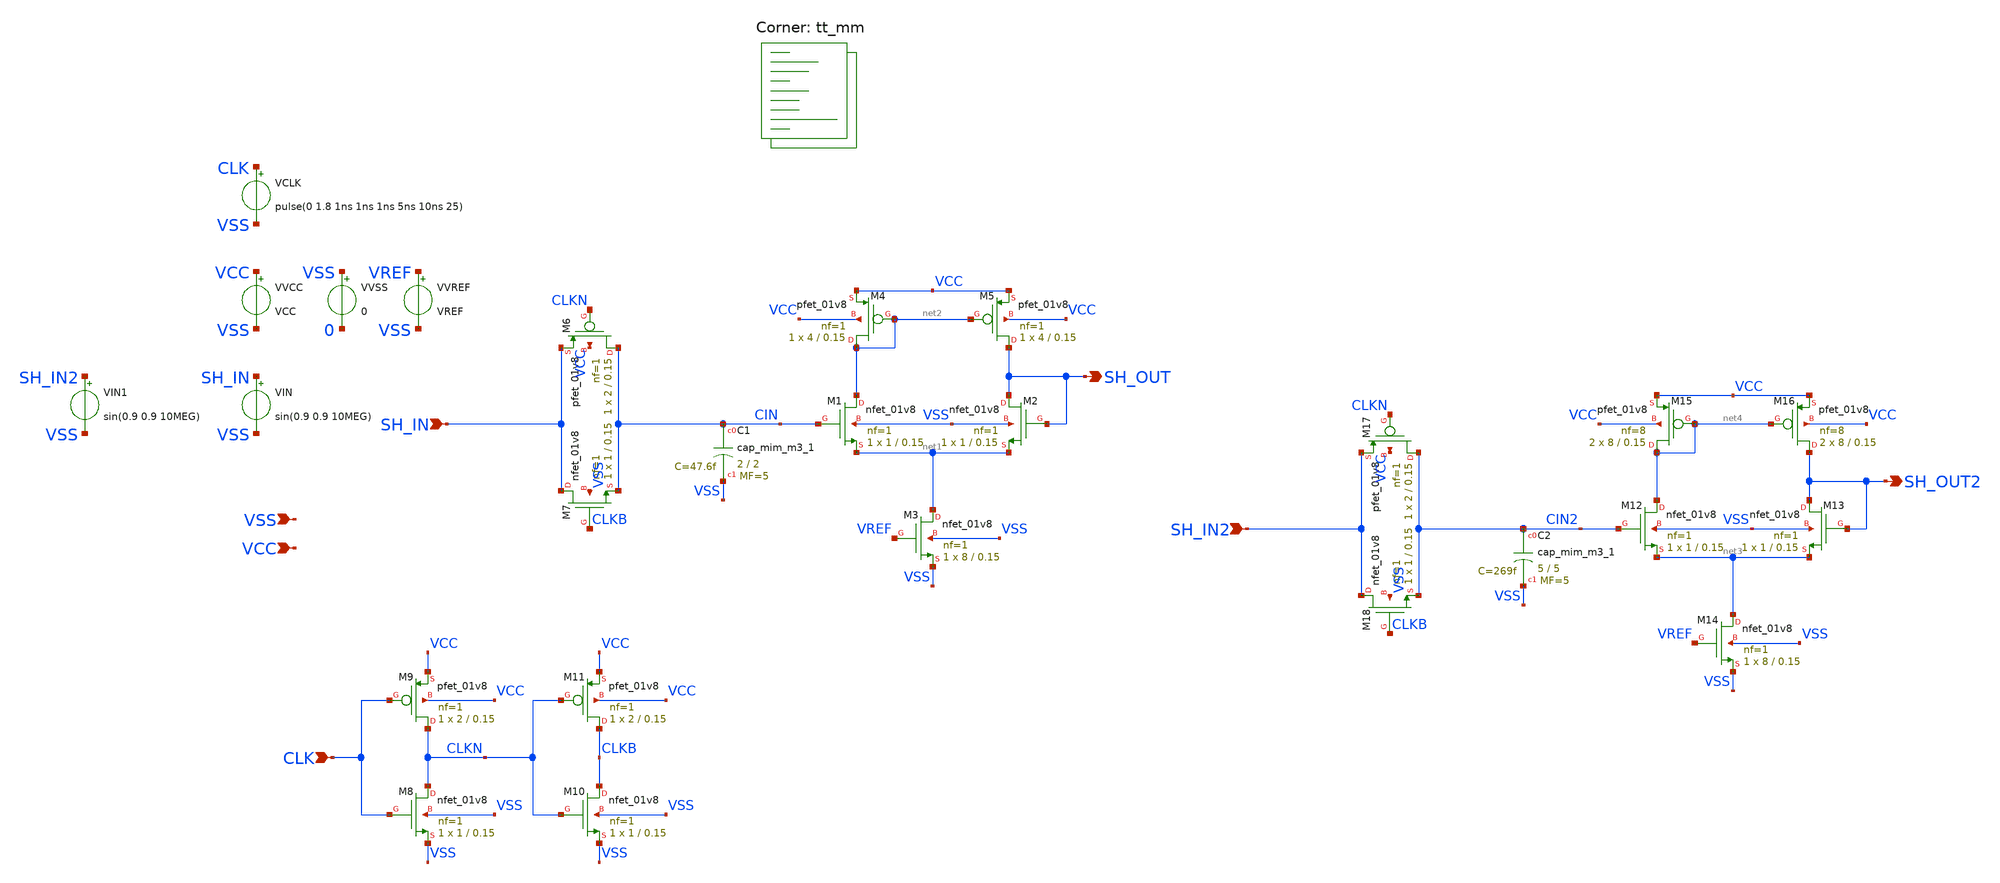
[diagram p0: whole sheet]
** sch_path: xschem/Sample_and_Hold.sch
**.subckt Sample_and_Hold SH_IN CLK SH_OUT VSS VCC SH_IN2 SH_OUT2
*.ipin SH_IN
*.ipin CLK
*.opin SH_OUT
*.ipin VSS
*.ipin VCC
*.ipin SH_IN2
*.opin SH_OUT2
XM1 net2 CIN net1 VSS sky130_fd_pr__nfet_01v8 L=0.15 W=1 nf=1 ad='int((nf+1)/2) * W/nf * 0.29' as='int((nf+2)/2) * W/nf * 0.29'
+ pd='2*int((nf+1)/2) * (W/nf + 0.29)' ps='2*int((nf+2)/2) * (W/nf + 0.29)' nrd='0.29 / W' nrs='0.29 / W'
+ sa=0 sb=0 sd=0 mult=1 m=1
XM2 SH_OUT SH_OUT net1 VSS sky130_fd_pr__nfet_01v8 L=0.15 W=1 nf=1 ad='int((nf+1)/2) * W/nf * 0.29' as='int((nf+2)/2) * W/nf * 0.29'
+ pd='2*int((nf+1)/2) * (W/nf + 0.29)' ps='2*int((nf+2)/2) * (W/nf + 0.29)' nrd='0.29 / W' nrs='0.29 / W'
+ sa=0 sb=0 sd=0 mult=1 m=1
XM3 net1 VREF VSS VSS sky130_fd_pr__nfet_01v8 L=0.15 W=8 nf=1 ad='int((nf+1)/2) * W/nf * 0.29' as='int((nf+2)/2) * W/nf * 0.29'
+ pd='2*int((nf+1)/2) * (W/nf + 0.29)' ps='2*int((nf+2)/2) * (W/nf + 0.29)' nrd='0.29 / W' nrs='0.29 / W'
+ sa=0 sb=0 sd=0 mult=1 m=1
XM4 net2 net2 VCC VCC sky130_fd_pr__pfet_01v8 L=0.15 W=4 nf=1 ad='int((nf+1)/2) * W/nf * 0.29' as='int((nf+2)/2) * W/nf * 0.29'
+ pd='2*int((nf+1)/2) * (W/nf + 0.29)' ps='2*int((nf+2)/2) * (W/nf + 0.29)' nrd='0.29 / W' nrs='0.29 / W'
+ sa=0 sb=0 sd=0 mult=1 m=1
XM5 SH_OUT net2 VCC VCC sky130_fd_pr__pfet_01v8 L=0.15 W=4 nf=1 ad='int((nf+1)/2) * W/nf * 0.29' as='int((nf+2)/2) * W/nf * 0.29'
+ pd='2*int((nf+1)/2) * (W/nf + 0.29)' ps='2*int((nf+2)/2) * (W/nf + 0.29)' nrd='0.29 / W' nrs='0.29 / W'
+ sa=0 sb=0 sd=0 mult=1 m=1
XC1 CIN VSS sky130_fd_pr__cap_mim_m3_1 W=2 L=2 MF=5 m=5
XM6 CIN CLKN SH_IN VCC sky130_fd_pr__pfet_01v8 L=0.15 W=2 nf=1 ad='int((nf+1)/2) * W/nf * 0.29' as='int((nf+2)/2) * W/nf * 0.29'
+ pd='2*int((nf+1)/2) * (W/nf + 0.29)' ps='2*int((nf+2)/2) * (W/nf + 0.29)' nrd='0.29 / W' nrs='0.29 / W'
+ sa=0 sb=0 sd=0 mult=1 m=1
XM7 SH_IN CLKB CIN VSS sky130_fd_pr__nfet_01v8 L=0.15 W=1 nf=1 ad='int((nf+1)/2) * W/nf * 0.29' as='int((nf+2)/2) * W/nf * 0.29'
+ pd='2*int((nf+1)/2) * (W/nf + 0.29)' ps='2*int((nf+2)/2) * (W/nf + 0.29)' nrd='0.29 / W' nrs='0.29 / W'
+ sa=0 sb=0 sd=0 mult=1 m=1
VCLK CLK VSS pulse(0 1.8 1ns 1ns 1ns 5ns 10ns 25)
VVCC VCC VSS VCC
VVSS VSS 0 0
VIN SH_IN VSS sin(0.9 0.9 10MEG)
VVREF VREF VSS VREF
XM8 CLKN CLK VSS VSS sky130_fd_pr__nfet_01v8 L=0.15 W=1 nf=1 ad='int((nf+1)/2) * W/nf * 0.29' as='int((nf+2)/2) * W/nf * 0.29'
+ pd='2*int((nf+1)/2) * (W/nf + 0.29)' ps='2*int((nf+2)/2) * (W/nf + 0.29)' nrd='0.29 / W' nrs='0.29 / W'
+ sa=0 sb=0 sd=0 mult=1 m=1
XM9 CLKN CLK VCC VCC sky130_fd_pr__pfet_01v8 L=0.15 W=2 nf=1 ad='int((nf+1)/2) * W/nf * 0.29' as='int((nf+2)/2) * W/nf * 0.29'
+ pd='2*int((nf+1)/2) * (W/nf + 0.29)' ps='2*int((nf+2)/2) * (W/nf + 0.29)' nrd='0.29 / W' nrs='0.29 / W'
+ sa=0 sb=0 sd=0 mult=1 m=1
XM10 CLKB CLKN VSS VSS sky130_fd_pr__nfet_01v8 L=0.15 W=1 nf=1 ad='int((nf+1)/2) * W/nf * 0.29' as='int((nf+2)/2) * W/nf * 0.29'
+ pd='2*int((nf+1)/2) * (W/nf + 0.29)' ps='2*int((nf+2)/2) * (W/nf + 0.29)' nrd='0.29 / W' nrs='0.29 / W'
+ sa=0 sb=0 sd=0 mult=1 m=1
XM11 CLKB CLKN VCC VCC sky130_fd_pr__pfet_01v8 L=0.15 W=2 nf=1 ad='int((nf+1)/2) * W/nf * 0.29' as='int((nf+2)/2) * W/nf * 0.29'
+ pd='2*int((nf+1)/2) * (W/nf + 0.29)' ps='2*int((nf+2)/2) * (W/nf + 0.29)' nrd='0.29 / W' nrs='0.29 / W'
+ sa=0 sb=0 sd=0 mult=1 m=1
XM12 net4 CIN2 net3 VSS sky130_fd_pr__nfet_01v8 L=0.15 W=1 nf=1 ad='int((nf+1)/2) * W/nf * 0.29' as='int((nf+2)/2) * W/nf * 0.29'
+ pd='2*int((nf+1)/2) * (W/nf + 0.29)' ps='2*int((nf+2)/2) * (W/nf + 0.29)' nrd='0.29 / W' nrs='0.29 / W'
+ sa=0 sb=0 sd=0 mult=1 m=1
XM13 SH_OUT2 SH_OUT2 net3 VSS sky130_fd_pr__nfet_01v8 L=0.15 W=1 nf=1 ad='int((nf+1)/2) * W/nf * 0.29'
+ as='int((nf+2)/2) * W/nf * 0.29' pd='2*int((nf+1)/2) * (W/nf + 0.29)' ps='2*int((nf+2)/2) * (W/nf + 0.29)'
+ nrd='0.29 / W' nrs='0.29 / W' sa=0 sb=0 sd=0 mult=1 m=1
XM14 net3 VREF VSS VSS sky130_fd_pr__nfet_01v8 L=0.15 W=8 nf=1 ad='int((nf+1)/2) * W/nf * 0.29' as='int((nf+2)/2) * W/nf * 0.29'
+ pd='2*int((nf+1)/2) * (W/nf + 0.29)' ps='2*int((nf+2)/2) * (W/nf + 0.29)' nrd='0.29 / W' nrs='0.29 / W'
+ sa=0 sb=0 sd=0 mult=1 m=1
XM15 net4 net4 VCC VCC sky130_fd_pr__pfet_01v8 L=0.15 W=8 nf=8 ad='int((nf+1)/2) * W/nf * 0.29' as='int((nf+2)/2) * W/nf * 0.29'
+ pd='2*int((nf+1)/2) * (W/nf + 0.29)' ps='2*int((nf+2)/2) * (W/nf + 0.29)' nrd='0.29 / W' nrs='0.29 / W'
+ sa=0 sb=0 sd=0 mult=2 m=2
XM16 SH_OUT2 net4 VCC VCC sky130_fd_pr__pfet_01v8 L=0.15 W=8 nf=8 ad='int((nf+1)/2) * W/nf * 0.29' as='int((nf+2)/2) * W/nf * 0.29'
+ pd='2*int((nf+1)/2) * (W/nf + 0.29)' ps='2*int((nf+2)/2) * (W/nf + 0.29)' nrd='0.29 / W' nrs='0.29 / W'
+ sa=0 sb=0 sd=0 mult=2 m=2
XC2 CIN2 VSS sky130_fd_pr__cap_mim_m3_1 W=5 L=5 MF=5 m=5
XM17 CIN2 CLKN SH_IN2 VCC sky130_fd_pr__pfet_01v8 L=0.15 W=2 nf=1 ad='int((nf+1)/2) * W/nf * 0.29' as='int((nf+2)/2) * W/nf * 0.29'
+ pd='2*int((nf+1)/2) * (W/nf + 0.29)' ps='2*int((nf+2)/2) * (W/nf + 0.29)' nrd='0.29 / W' nrs='0.29 / W'
+ sa=0 sb=0 sd=0 mult=1 m=1
XM18 SH_IN2 CLKB CIN2 VSS sky130_fd_pr__nfet_01v8 L=0.15 W=1 nf=1 ad='int((nf+1)/2) * W/nf * 0.29' as='int((nf+2)/2) * W/nf * 0.29'
+ pd='2*int((nf+1)/2) * (W/nf + 0.29)' ps='2*int((nf+2)/2) * (W/nf + 0.29)' nrd='0.29 / W' nrs='0.29 / W'
+ sa=0 sb=0 sd=0 mult=1 m=1
VIN1 SH_IN2 VSS sin(0.9 0.9 10MEG)
**** begin user architecture code


.option chgtol=4e-16 method=gear
.param VCC = 1.8
.param VREF = 1.8
.param temp = 25

.control
  setseed 8
  reset
  let run = 1
  save all
  op
  write Sample_and_Hold.raw
  reset
  set appendwrite
  save SH_IN SH_OUT CLK CIN SH_IN2 SH_OUT2 CIN2
  tran 0.1n 250n uic
  write Sample_and_Hold.raw
  let run = run + 1
  reset
  quit 0
.endc

.lib $::SKYWATER_MODELS/sky130.lib.spice tt_mm
**** end user architecture code
**.ends
.end
